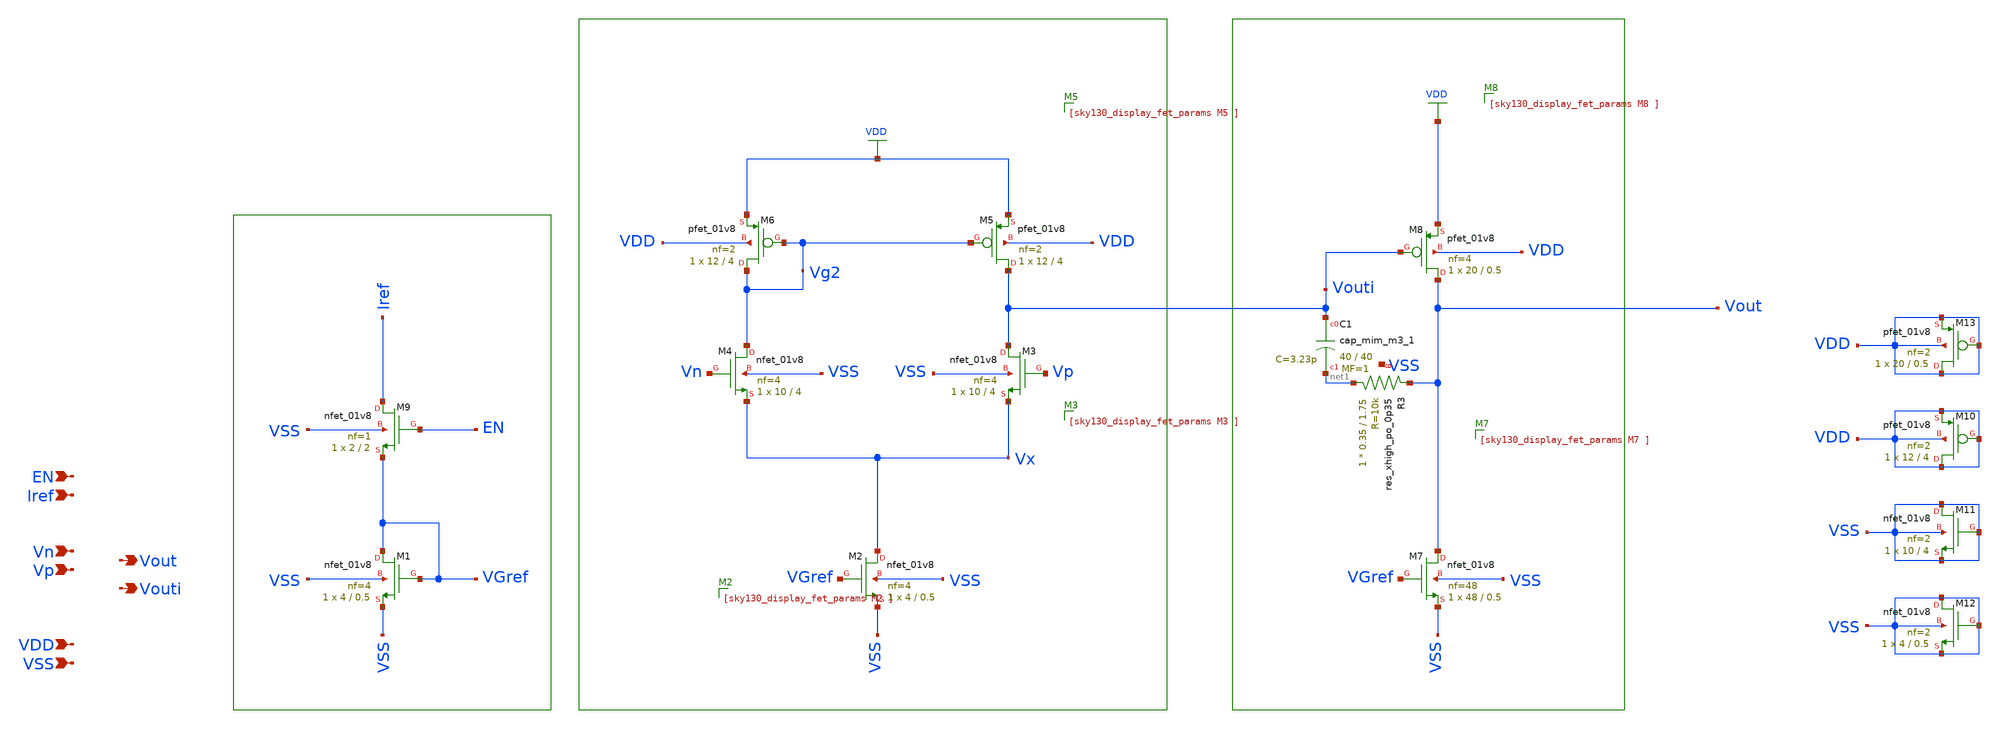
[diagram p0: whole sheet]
** sch_path: xschem/opamp.sch
**.subckt opamp VSS Vp Vout Vn VDD Iref Vouti EN
*.ipin VSS
*.ipin Vp
*.opin Vout
*.ipin Vn
*.ipin VDD
*.ipin Iref
*.opin Vouti
*.ipin EN
XM1 VGref VGref VSS VSS sky130_fd_pr__nfet_01v8 L=0.5 W=4 nf=4 ad='int((4 + 1)/2) * 4 / 4 * 0.29' as='int((4 + 2)/2) * 4 / 4 * 0.29'
+ pd='2*int((4 + 1)/2) * (4 / 4 + 0.29)' ps='2*int((4 + 2)/2) * (4 / 4 + 0.29)' nrd='0.29 / 4 ' nrs='0.29 / 4 '
+ sa=0 sb=0 sd=0 mult=1 m=1
XM2 Vx VGref VSS VSS sky130_fd_pr__nfet_01v8 L=0.5 W=4 nf=4 ad='int((4 + 1)/2) * 4 / 4 * 0.29' as='int((4 + 2)/2) * 4 / 4 * 0.29'
+ pd='2*int((4 + 1)/2) * (4 / 4 + 0.29)' ps='2*int((4 + 2)/2) * (4 / 4 + 0.29)' nrd='0.29 / 4 ' nrs='0.29 / 4 '
+ sa=0 sb=0 sd=0 mult=1 m=1
XM3 Vouti Vp Vx VSS sky130_fd_pr__nfet_01v8 L=4 W=10 nf=4 ad='int((4 + 1)/2) * 10 / 4 * 0.29' as='int((4 + 2)/2) * 10 / 4 * 0.29'
+ pd='2*int((4 + 1)/2) * (10 / 4 + 0.29)' ps='2*int((4 + 2)/2) * (10 / 4 + 0.29)' nrd='0.29 / 10 ' nrs='0.29 / 10 '
+ sa=0 sb=0 sd=0 mult=1 m=1
XM4 Vg2 Vn Vx VSS sky130_fd_pr__nfet_01v8 L=4 W=10 nf=4 ad='int((4 + 1)/2) * 10 / 4 * 0.29' as='int((4 + 2)/2) * 10 / 4 * 0.29'
+ pd='2*int((4 + 1)/2) * (10 / 4 + 0.29)' ps='2*int((4 + 2)/2) * (10 / 4 + 0.29)' nrd='0.29 / 10 ' nrs='0.29 / 10 '
+ sa=0 sb=0 sd=0 mult=1 m=1
XM5 Vouti Vg2 VDD VDD sky130_fd_pr__pfet_01v8 L=4 W=12 nf=2 ad='int((2 + 1)/2) * 12 / 2 * 0.29' as='int((2 + 2)/2) * 12 / 2 * 0.29'
+ pd='2*int((2 + 1)/2) * (12 / 2 + 0.29)' ps='2*int((2 + 2)/2) * (12 / 2 + 0.29)' nrd='0.29 / 12 ' nrs='0.29 / 12 '
+ sa=0 sb=0 sd=0 mult=1 m=1
XM6 Vg2 Vg2 VDD VDD sky130_fd_pr__pfet_01v8 L=4 W=12 nf=2 ad='int((2 + 1)/2) * 12 / 2 * 0.29' as='int((2 + 2)/2) * 12 / 2 * 0.29'
+ pd='2*int((2 + 1)/2) * (12 / 2 + 0.29)' ps='2*int((2 + 2)/2) * (12 / 2 + 0.29)' nrd='0.29 / 12 ' nrs='0.29 / 12 '
+ sa=0 sb=0 sd=0 mult=1 m=1
XM7 Vout VGref VSS VSS sky130_fd_pr__nfet_01v8 L=0.5 W=48 nf=48 ad='int((48 + 1)/2) * 48 / 48 * 0.29'
+ as='int((48 + 2)/2) * 48 / 48 * 0.29' pd='2*int((48 + 1)/2) * (48 / 48 + 0.29)' ps='2*int((48 + 2)/2) * (48 / 48 + 0.29)'
+ nrd='0.29 / 48 ' nrs='0.29 / 48 ' sa=0 sb=0 sd=0 mult=1 m=1
XM8 Vout Vouti VDD VDD sky130_fd_pr__pfet_01v8 L=0.5 W=20 nf=4 ad='int((4 + 1)/2) * 20 / 4 * 0.29' as='int((4 + 2)/2) * 20 / 4 * 0.29'
+ pd='2*int((4 + 1)/2) * (20 / 4 + 0.29)' ps='2*int((4 + 2)/2) * (20 / 4 + 0.29)' nrd='0.29 / 20 ' nrs='0.29 / 20 '
+ sa=0 sb=0 sd=0 mult=1 m=1
XM9 Iref EN VGref VSS sky130_fd_pr__nfet_01v8 L=2 W=2 nf=1 ad='int((1 + 1)/2) * 2 / 1 * 0.29' as='int((1 + 2)/2) * 2 / 1 * 0.29'
+ pd='2*int((1 + 1)/2) * (2 / 1 + 0.29)' ps='2*int((1 + 2)/2) * (2 / 1 + 0.29)' nrd='0.29 / 2 ' nrs='0.29 / 2 '
+ sa=0 sb=0 sd=0 mult=1 m=1
XC1 Vouti net1 sky130_fd_pr__cap_mim_m3_1 W=40 L=40 MF=1 m=1
XR3 net1 Vout VSS sky130_fd_pr__res_xhigh_po_0p35 L=1.75 mult=1 m=1
XM11 VSS VSS VSS VSS sky130_fd_pr__nfet_01v8 L=4 W=10 nf=2 ad='int((2 + 1)/2) * 10 / 2 * 0.29' as='int((2 + 2)/2) * 10 / 2 * 0.29'
+ pd='2*int((2 + 1)/2) * (10 / 2 + 0.29)' ps='2*int((2 + 2)/2) * (10 / 2 + 0.29)' nrd='0.29 / 10 ' nrs='0.29 / 10 '
+ sa=0 sb=0 sd=0 mult=1 m=1
XM12 VSS VSS VSS VSS sky130_fd_pr__nfet_01v8 L=0.5 W=4 nf=2 ad='int((2 + 1)/2) * 4 / 2 * 0.29' as='int((2 + 2)/2) * 4 / 2 * 0.29'
+ pd='2*int((2 + 1)/2) * (4 / 2 + 0.29)' ps='2*int((2 + 2)/2) * (4 / 2 + 0.29)' nrd='0.29 / 4 ' nrs='0.29 / 4 '
+ sa=0 sb=0 sd=0 mult=1 m=1
XM10 VDD VDD VDD VDD sky130_fd_pr__pfet_01v8 L=4 W=12 nf=2 ad='int((2 + 1)/2) * 12 / 2 * 0.29' as='int((2 + 2)/2) * 12 / 2 * 0.29'
+ pd='2*int((2 + 1)/2) * (12 / 2 + 0.29)' ps='2*int((2 + 2)/2) * (12 / 2 + 0.29)' nrd='0.29 / 12 ' nrs='0.29 / 12 '
+ sa=0 sb=0 sd=0 mult=1 m=1
XM13 VDD VDD VDD VDD sky130_fd_pr__pfet_01v8 L=0.5 W=20 nf=2 ad='int((2 + 1)/2) * 20 / 2 * 0.29' as='int((2 + 2)/2) * 20 / 2 * 0.29'
+ pd='2*int((2 + 1)/2) * (20 / 2 + 0.29)' ps='2*int((2 + 2)/2) * (20 / 2 + 0.29)' nrd='0.29 / 20 ' nrs='0.29 / 20 '
+ sa=0 sb=0 sd=0 mult=1 m=1
**.ends
.GLOBAL VDD
.end
